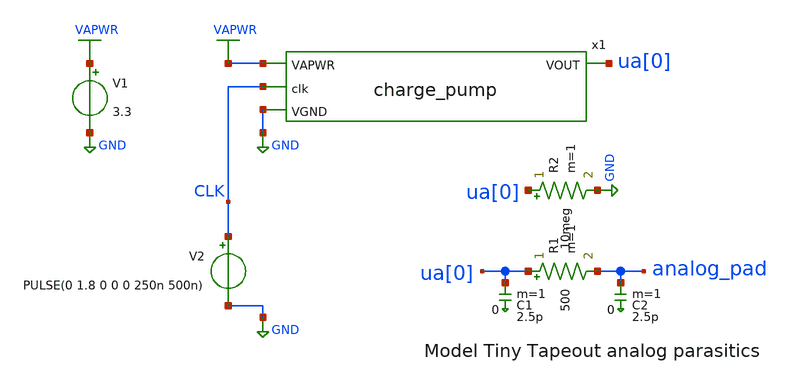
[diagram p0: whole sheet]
** sch_path: xschem/charge_pump_tb.sch
**.subckt charge_pump_tb
V1 VAPWR GND 3.3
V2 CLK GND PULSE(0 1.8 0 0 0 250n 500n)
R1 ua[0] analog_pad 500 m=1
C1 ua[0] 0 2.5p m=1
C2 analog_pad 0 2.5p m=1
x1 VAPWR ua[0] CLK GND charge_pump
R2 ua[0] GND 10meg m=1
**** begin user architecture code

** opencircuitdesign pdks install
.lib $::SKYWATER_MODELS/sky130.lib.spice tt
.include ../../spice/charge_pump/pex/charge_pump.spice
*.include ../../spice/charge_pump/sch/charge_pump.spice




.tran 10n 100u
.save all
.options savecurrents

.control
run
write pump_tb.raw
.endc


**** end user architecture code
**.ends
.GLOBAL GND
.GLOBAL VAPWR
.end
